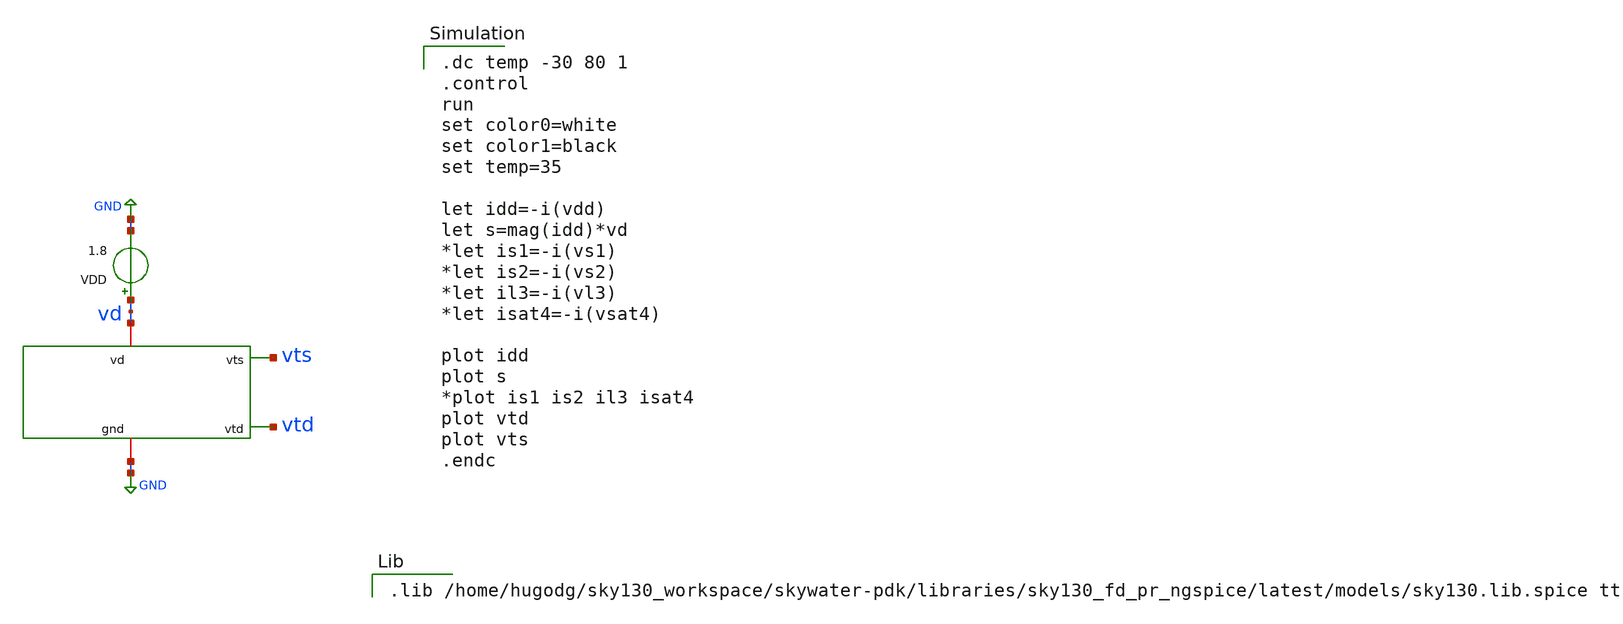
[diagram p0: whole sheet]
** sch_path: sensor/xschem/temp-tb-short.sch
**.subckt temp-tb-short
VDD vd GND 1.8
x1 vd vts vtd GND sensor
**** begin user architecture code

.dc temp -30 80 1
.control
run
set color0=white
set color1=black
set temp=35

let idd=-i(vdd)
let s=mag(idd)*vd
*let is1=-i(vs1)
*let is2=-i(vs2)
*let il3=-i(vl3)
*let isat4=-i(vsat4)

plot idd
plot s
*plot is1 is2 il3 isat4
plot vtd
plot vts
.endc



.lib /home/hugodg/sky130_workspace/skywater-pdk/libraries/sky130_fd_pr_ngspice/latest/models/sky130.lib.spice tt

**** end user architecture code
**.ends

* expanding   symbol:  /home/hugodg/projects-sky130/temp-sensor/sensor/xschem/sensor.sym # of pins=4
** sym_path: sensor/xschem/sensor.sym
** sch_path: sensor/xschem/sensor.sch
.subckt sensor vd vts vtd gnd
*.iopin vd
*.iopin gnd
*.opin vts
*.opin vtd
XP6 vtd vtd vts vts sky130_fd_pr__pfet_01v8 L=1 W=96 nf=12 ad='int((nf+1)/2) * W/nf * 0.29' as='int((nf+2)/2) * W/nf * 0.29'
+ pd='2*int((nf+1)/2) * (W/nf + 0.29)' ps='2*int((nf+2)/2) * (W/nf + 0.29)' nrd='0.29 / W' nrs='0.29 / W'
+ sa=0 sb=0 sd=0 mult=1 m=1
XN1 net1 net2 gnd gnd sky130_fd_pr__nfet_01v8 L=28 W=1 nf=1 ad='int((nf+1)/2) * W/nf * 0.29' as='int((nf+2)/2) * W/nf * 0.29'
+ pd='2*int((nf+1)/2) * (W/nf + 0.29)' ps='2*int((nf+2)/2) * (W/nf + 0.29)' nrd='0.29 / W' nrs='0.29 / W'
+ sa=0 sb=0 sd=0 mult=1 m=1
XP3 net3 vtd vd vd sky130_fd_pr__pfet_01v8 L=1 W=32 nf=4 ad='int((nf+1)/2) * W/nf * 0.29' as='int((nf+2)/2) * W/nf * 0.29'
+ pd='2*int((nf+1)/2) * (W/nf + 0.29)' ps='2*int((nf+2)/2) * (W/nf + 0.29)' nrd='0.29 / W' nrs='0.29 / W'
+ sa=0 sb=0 sd=0 mult=1 m=1
XP1 net1 net1 vd vd sky130_fd_pr__pfet_01v8 L=1 W=8 nf=1 ad='int((nf+1)/2) * W/nf * 0.29' as='int((nf+2)/2) * W/nf * 0.29'
+ pd='2*int((nf+1)/2) * (W/nf + 0.29)' ps='2*int((nf+2)/2) * (W/nf + 0.29)' nrd='0.29 / W' nrs='0.29 / W'
+ sa=0 sb=0 sd=0 mult=1 m=1
XP2 net4 net1 net3 net3 sky130_fd_pr__pfet_01v8 L=1 W=64 nf=8 ad='int((nf+1)/2) * W/nf * 0.29' as='int((nf+2)/2) * W/nf * 0.29'
+ pd='2*int((nf+1)/2) * (W/nf + 0.29)' ps='2*int((nf+2)/2) * (W/nf + 0.29)' nrd='0.29 / W' nrs='0.29 / W'
+ sa=0 sb=0 sd=0 mult=1 m=1
XP4 vts vtd vd vd sky130_fd_pr__pfet_01v8 L=8 W=32 nf=4 ad='int((nf+1)/2) * W/nf * 0.29' as='int((nf+2)/2) * W/nf * 0.29'
+ pd='2*int((nf+1)/2) * (W/nf + 0.29)' ps='2*int((nf+2)/2) * (W/nf + 0.29)' nrd='0.29 / W' nrs='0.29 / W'
+ sa=0 sb=0 sd=0 mult=1 m=1
XN2 net2 net2 gnd gnd sky130_fd_pr__nfet_01v8 L=28 W=1 nf=1 ad='int((nf+1)/2) * W/nf * 0.29' as='int((nf+2)/2) * W/nf * 0.29'
+ pd='2*int((nf+1)/2) * (W/nf + 0.29)' ps='2*int((nf+2)/2) * (W/nf + 0.29)' nrd='0.29 / W' nrs='0.29 / W'
+ sa=0 sb=0 sd=0 mult=1 m=1
XN3 vtd net2 gnd gnd sky130_fd_pr__nfet_01v8 L=28 W=1 nf=1 ad='int((nf+1)/2) * W/nf * 0.29' as='int((nf+2)/2) * W/nf * 0.29'
+ pd='2*int((nf+1)/2) * (W/nf + 0.29)' ps='2*int((nf+2)/2) * (W/nf + 0.29)' nrd='0.29 / W' nrs='0.29 / W'
+ sa=0 sb=0 sd=0 mult=1 m=1
XP5 net2 vtd net4 net4 sky130_fd_pr__pfet_01v8 L=1 W=24 nf=3 ad='int((nf+1)/2) * W/nf * 0.29' as='int((nf+2)/2) * W/nf * 0.29'
+ pd='2*int((nf+1)/2) * (W/nf + 0.29)' ps='2*int((nf+2)/2) * (W/nf + 0.29)' nrd='0.29 / W' nrs='0.29 / W'
+ sa=0 sb=0 sd=0 mult=1 m=1
.ends

.GLOBAL GND
.end
